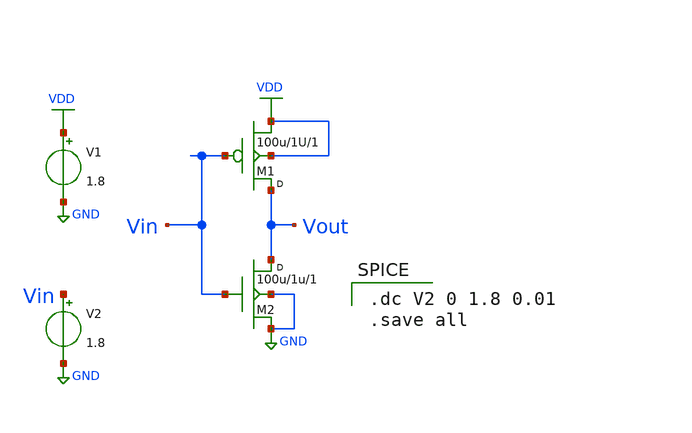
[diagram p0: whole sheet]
** sch_path: CMOS Inverter/cmos invt.sch
**.subckt cmos invt
V1 VDD GND 1.8
V2 Vin GND 1.8
M1 Vout Vin VDD VDD irf5305 w=100u l=1U m=1
M2 Vout Vin GND GND irf540 w=100u l=1u m=1
**** begin user architecture code

.dc V2 0 1.8 0.01
.save all


.MODEL IRF5305 PMOS (VT0=-0.7 KP=2e-3)
.MODEL IRF540 NMOS (VT0=0.7 KP=4e-3)

**** end user architecture code
**.ends
.GLOBAL GND
.GLOBAL VDD
.end
